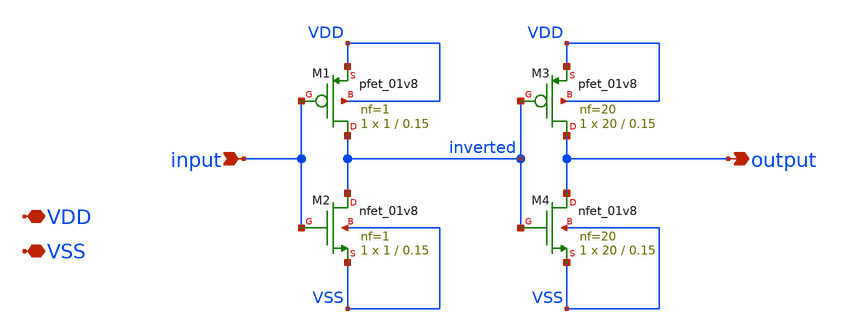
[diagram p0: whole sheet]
** sch_path: xschem/double_inverter.sch
**.subckt double_inverter VDD VSS input output
*.iopin VDD
*.iopin VSS
*.ipin input
*.opin output
XM1 inverted input VDD VDD sky130_fd_pr__pfet_01v8 L=0.15 W=1 nf=1 ad='int((nf+1)/2) * W/nf * 0.29' as='int((nf+2)/2) * W/nf * 0.29'
+ pd='2*int((nf+1)/2) * (W/nf + 0.29)' ps='2*int((nf+2)/2) * (W/nf + 0.29)' nrd='0.29 / W' nrs='0.29 / W'
+ sa=0 sb=0 sd=0 mult=1 m=1
XM2 inverted input VSS VSS sky130_fd_pr__nfet_01v8 L=0.15 W=1 nf=1 ad='int((nf+1)/2) * W/nf * 0.29' as='int((nf+2)/2) * W/nf * 0.29'
+ pd='2*int((nf+1)/2) * (W/nf + 0.29)' ps='2*int((nf+2)/2) * (W/nf + 0.29)' nrd='0.29 / W' nrs='0.29 / W'
+ sa=0 sb=0 sd=0 mult=1 m=1
XM3 output inverted VDD VDD sky130_fd_pr__pfet_01v8 L=0.15 W=20 nf=20 ad='int((nf+1)/2) * W/nf * 0.29'
+ as='int((nf+2)/2) * W/nf * 0.29' pd='2*int((nf+1)/2) * (W/nf + 0.29)' ps='2*int((nf+2)/2) * (W/nf + 0.29)'
+ nrd='0.29 / W' nrs='0.29 / W' sa=0 sb=0 sd=0 mult=1 m=1
XM4 output inverted VSS VSS sky130_fd_pr__nfet_01v8 L=0.15 W=20 nf=20 ad='int((nf+1)/2) * W/nf * 0.29'
+ as='int((nf+2)/2) * W/nf * 0.29' pd='2*int((nf+1)/2) * (W/nf + 0.29)' ps='2*int((nf+2)/2) * (W/nf + 0.29)'
+ nrd='0.29 / W' nrs='0.29 / W' sa=0 sb=0 sd=0 mult=1 m=1
**.ends
.end
